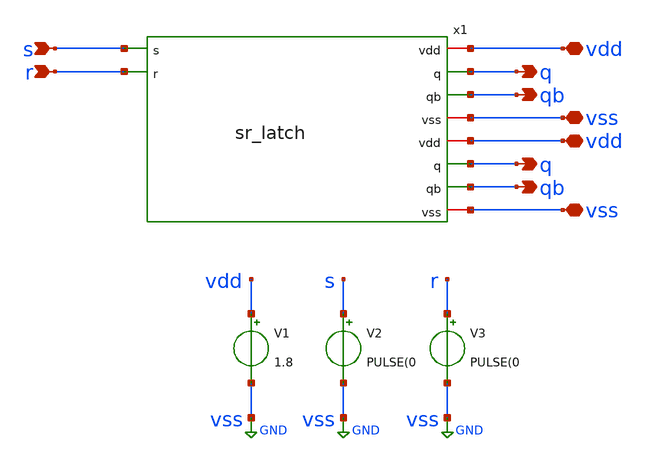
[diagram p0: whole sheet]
** sch_path: xschem/sr_latch_tbh.sch
**.subckt sr_latch_tbh s r vdd q vdd vss vss q qb qb
*.ipin s
*.ipin r
*.iopin vdd
*.opin q
*.iopin vdd
*.iopin vss
*.iopin vss
*.opin q
*.opin qb
*.opin qb
x1 s vdd q qb vss r sr_latch
V1 vdd vss 1.8
V2 s vss PULSE(0
V3 r vss PULSE(0
**** begin user architecture code


.lib /home/eprempeh/pdk/sky130A/libs.tech/ngspice/sky130.lib.spice tt
.control
  tran 0.1n 500n
  plot v(s) v(r) v(q) v(qb)
.endc
.endc


**** end user architecture code
**.ends

* expanding   symbol:  sr_latch.sym # of pins=10
** sym_path: xschem/sr_latch.sym
** sch_path: xschem/sr_latch.sch
.subckt sr_latch s vdd q qb vss r
*.ipin s
*.opin q
*.ipin r
*.opin qb
*.opin qb
*.opin q
*.iopin vdd
*.iopin vss
*.iopin vdd
*.iopin vss
x1 vdd s q qb vss nor_gate
x2 vdd q qb r vss nor_gate
.ends


* expanding   symbol:  nor_gate.sym # of pins=5
** sym_path: xschem/nor_gate.sym
** sch_path: xschem/nor_gate.sch
.subckt nor_gate vdd a y b vss
*.ipin a
*.ipin b
*.opin y
*.iopin vdd
*.iopin vss
XM1 net1 a vdd vdd sky130_fd_pr__pfet_01v8 L=0.15 W=1.5 nf=1 ad='int((nf+1)/2) * W/nf * 0.29' as='int((nf+2)/2) * W/nf * 0.29'
+ pd='2*int((nf+1)/2) * (W/nf + 0.29)' ps='2*int((nf+2)/2) * (W/nf + 0.29)' nrd='0.29 / W' nrs='0.29 / W'
+ sa=0 sb=0 sd=0 mult=1 m=1
XM2 y b net1 vdd sky130_fd_pr__pfet_01v8 L=0.15 W=1.5 nf=1 ad='int((nf+1)/2) * W/nf * 0.29' as='int((nf+2)/2) * W/nf * 0.29'
+ pd='2*int((nf+1)/2) * (W/nf + 0.29)' ps='2*int((nf+2)/2) * (W/nf + 0.29)' nrd='0.29 / W' nrs='0.29 / W'
+ sa=0 sb=0 sd=0 mult=1 m=1
XM3 y a vss vss sky130_fd_pr__nfet_01v8 L=0.15 W=0.75 nf=1 ad='int((nf+1)/2) * W/nf * 0.29' as='int((nf+2)/2) * W/nf * 0.29'
+ pd='2*int((nf+1)/2) * (W/nf + 0.29)' ps='2*int((nf+2)/2) * (W/nf + 0.29)' nrd='0.29 / W' nrs='0.29 / W'
+ sa=0 sb=0 sd=0 mult=1 m=1
XM4 y b vss vss sky130_fd_pr__nfet_01v8 L=0.15 W=0.75 nf=1 ad='int((nf+1)/2) * W/nf * 0.29' as='int((nf+2)/2) * W/nf * 0.29'
+ pd='2*int((nf+1)/2) * (W/nf + 0.29)' ps='2*int((nf+2)/2) * (W/nf + 0.29)' nrd='0.29 / W' nrs='0.29 / W'
+ sa=0 sb=0 sd=0 mult=1 m=1
.ends

.GLOBAL GND
.end
